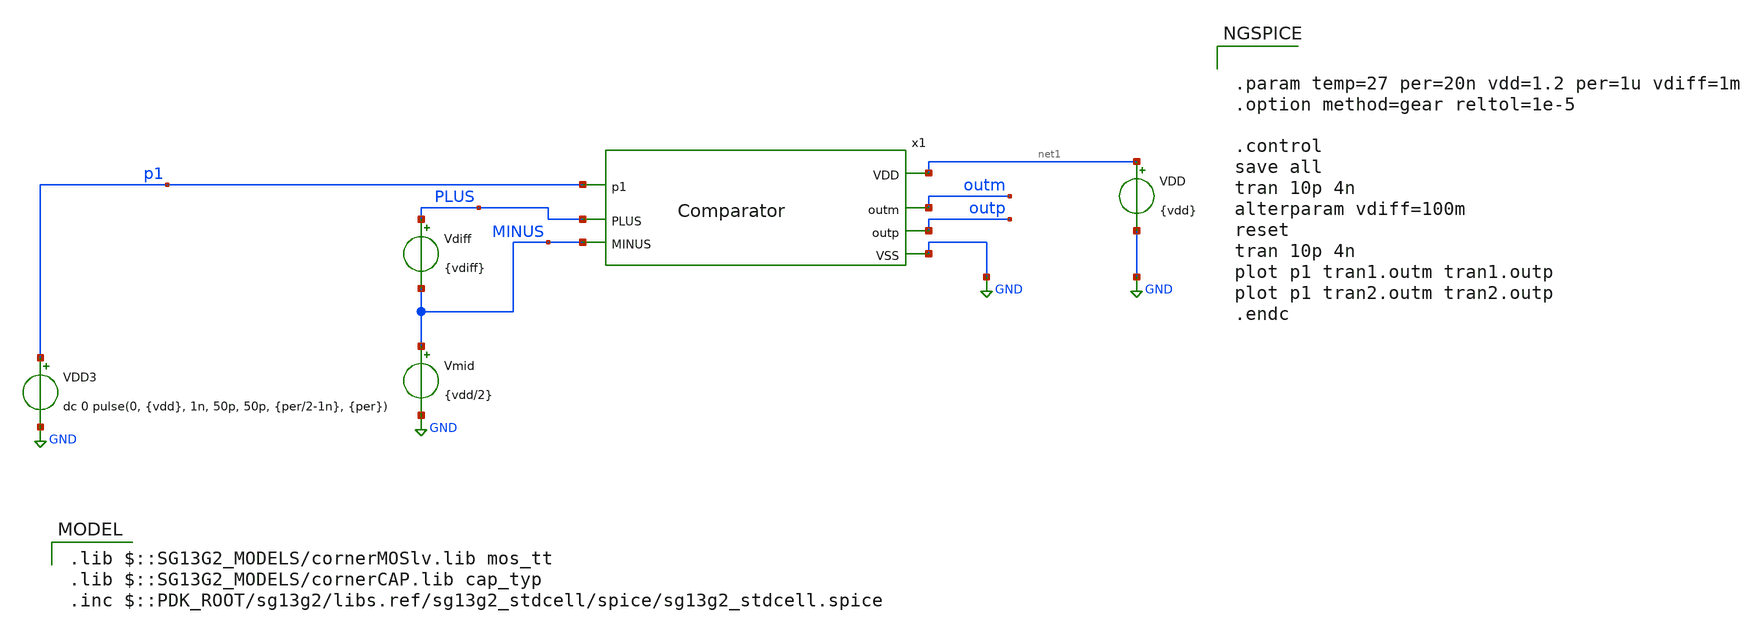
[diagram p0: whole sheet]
** sch_path: DSM/Schematics/Sneha/tb_Comparator.sch
**.subckt tb_Comparator
VDD net1 GND {vdd}
Vdiff PLUS MINUS {vdiff}
Vmid MINUS GND {vdd/2}
VDD3 p1 GND dc 0 pulse(0, {vdd}, 1n, 50p, 50p, {per/2-1n}, {per})
x1 net1 p1 outm outp MINUS PLUS GND Comparator
**** begin user architecture code


.param temp=27 per=20n vdd=1.2 per=1u vdiff=1m
.option method=gear reltol=1e-5

.control
save all
tran 10p 4n
alterparam vdiff=100m
reset
tran 10p 4n
plot p1 tran1.outm tran1.outp
plot p1 tran2.outm tran2.outp
.endc


 .lib $::SG13G2_MODELS/cornerMOSlv.lib mos_tt
.lib $::SG13G2_MODELS/cornerCAP.lib cap_typ
.inc $::PDK_ROOT/sg13g2/libs.ref/sg13g2_stdcell/spice/sg13g2_stdcell.spice

**** end user architecture code
**.ends
.GLOBAL GND
.end
